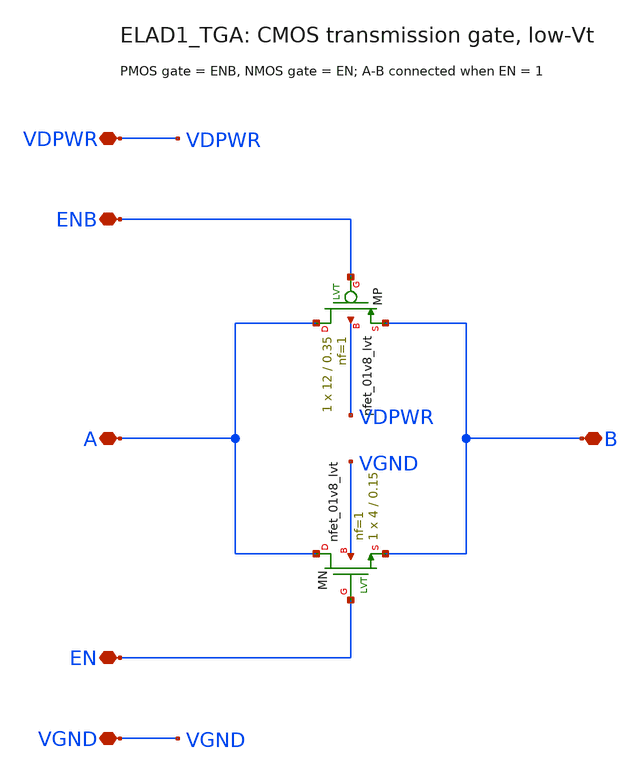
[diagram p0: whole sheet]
** sch_path: cells/ELAD1_TGA/schematic/ELAD1_TGA.sch
**.subckt ELAD1_TGA A B EN ENB VDPWR VGND
*.iopin A
*.iopin B
*.iopin EN
*.iopin ENB
*.iopin VDPWR
*.iopin VGND
XMP A ENB B VDPWR sky130_fd_pr__pfet_01v8_lvt L=0.35 W=12 nf=1 ad='int((1 + 1)/2) * 12 / 1 * 0.29' as='int((1 + 2)/2) * 12 / 1 * 0.29'
+ pd='2*int((1 + 1)/2) * (12 / 1 + 0.29)' ps='2*int((1 + 2)/2) * (12 / 1 + 0.29)' nrd='0.29 / 12 ' nrs='0.29 / 12 '
+ sa=0 sb=0 sd=0 mult=1 m=1
XMN A EN B VGND sky130_fd_pr__nfet_01v8_lvt L=0.15 W=4 nf=1 ad='int((1 + 1)/2) * 4 / 1 * 0.29' as='int((1 + 2)/2) * 4 / 1 * 0.29'
+ pd='2*int((1 + 1)/2) * (4 / 1 + 0.29)' ps='2*int((1 + 2)/2) * (4 / 1 + 0.29)' nrd='0.29 / 4 ' nrs='0.29 / 4 '
+ sa=0 sb=0 sd=0 mult=1 m=1
**.ends
.end
